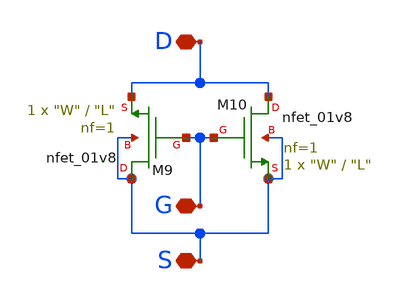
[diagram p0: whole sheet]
** sch_path: xschem/lib/nfet3_01v8_2.sch
**.subckt nfet3_01v8_2 D G S
*.iopin D
*.iopin G
*.iopin S
XM9 S G D S sky130_fd_pr__nfet_01v8 L="L" W="W" nf=1 ad='int((nf+1)/2) * W/nf * 0.29' as='int((nf+2)/2) * W/nf * 0.29'
+ pd='2*int((nf+1)/2) * (W/nf + 0.29)' ps='2*int((nf+2)/2) * (W/nf + 0.29)' nrd='0.29 / W' nrs='0.29 / W'
+ sa=0 sb=0 sd=0 mult=1 m=1
XM10 D G S S sky130_fd_pr__nfet_01v8 L="L" W="W" nf=1 ad='int((nf+1)/2) * W/nf * 0.29' as='int((nf+2)/2) * W/nf * 0.29'
+ pd='2*int((nf+1)/2) * (W/nf + 0.29)' ps='2*int((nf+2)/2) * (W/nf + 0.29)' nrd='0.29 / W' nrs='0.29 / W'
+ sa=0 sb=0 sd=0 mult=1 m=1
**.ends
.end
